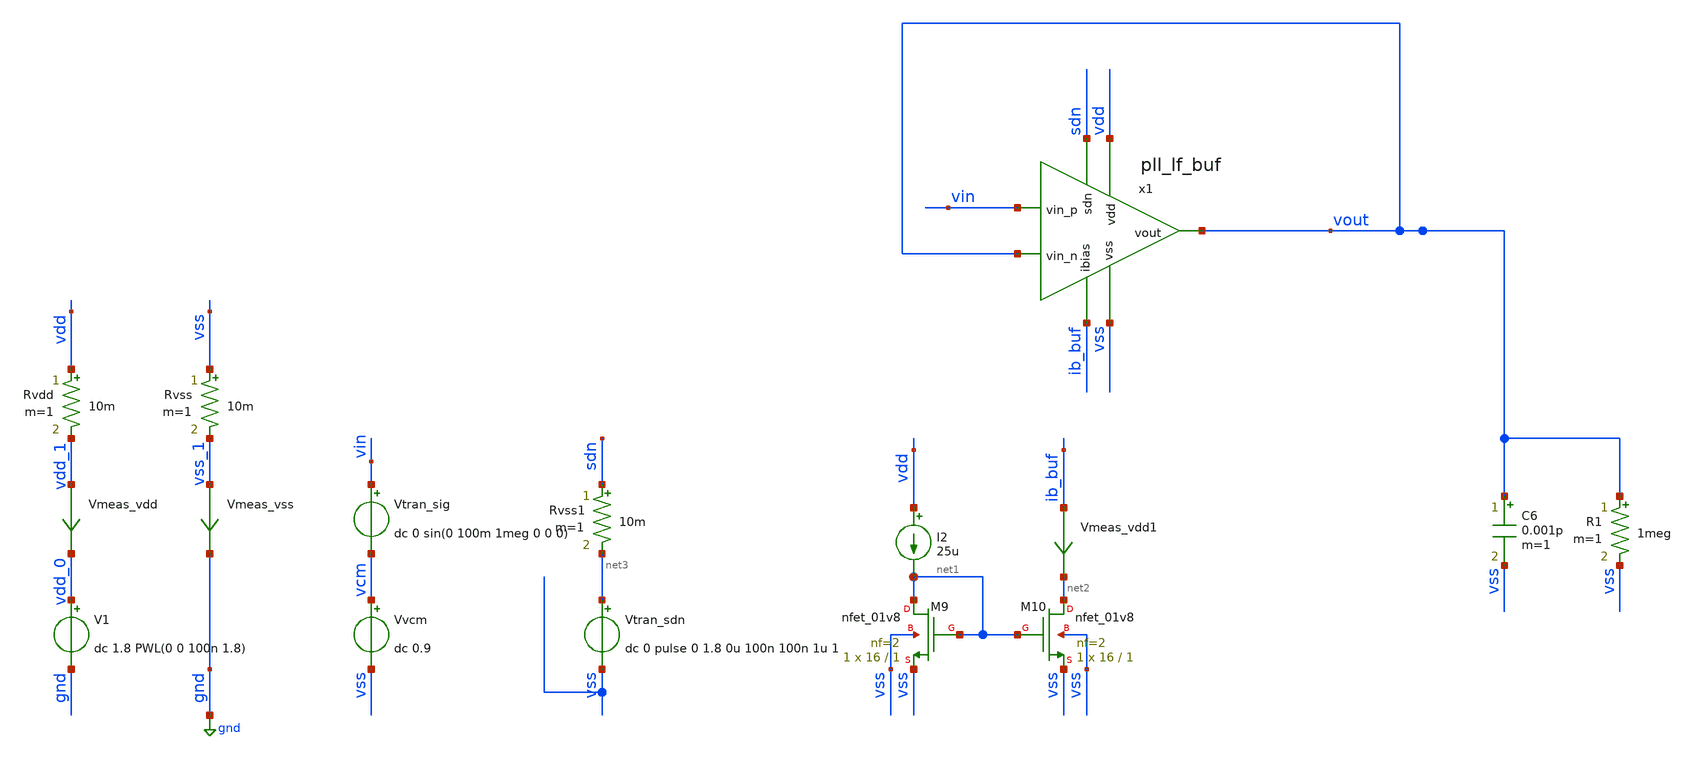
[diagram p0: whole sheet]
** sch_path: pll/pll_lf_buf/simulation/pll_lf_buf_tb_tran.sch
**.subckt pll_lf_buf_tb_tran
Vvcm vcm vss dc 0.9
C6 vout vss 0.001p m=1
Vtran_sig vin vcm dc 0 sin(0 100m 1meg 0 0 0)
Vtran_sdn net3 vss dc 0 pulse 0 1.8 0u 100n 100n 1u 1
V1 vdd_0 gnd dc 1.8 PWL(0 0 100n 1.8)
Vmeas_vdd vdd_1 vdd_0 0
.save i(vmeas_vdd)
Vmeas_vss vss_1 gnd 0
.save i(vmeas_vss)
Rvdd vdd vdd_1 10m m=1
Rvss vss vss_1 10m m=1
I2 vdd net1 25u
R1 vout vss 1meg m=1
Rvss1 sdn net3 10m m=1
XM9 net1 net1 vss vss sky130_fd_pr__nfet_01v8 L=1 W=16 nf=2 ad='int((nf+1)/2) * W/nf * 0.29' as='int((nf+2)/2) * W/nf * 0.29'
+ pd='2*int((nf+1)/2) * (W/nf + 0.29)' ps='2*int((nf+2)/2) * (W/nf + 0.29)' nrd='0.29 / W' nrs='0.29 / W'
+ sa=0 sb=0 sd=0 mult=1 m=1
XM10 net2 net1 vss vss sky130_fd_pr__nfet_01v8 L=1 W=16 nf=2 ad='int((nf+1)/2) * W/nf * 0.29' as='int((nf+2)/2) * W/nf * 0.29'
+ pd='2*int((nf+1)/2) * (W/nf + 0.29)' ps='2*int((nf+2)/2) * (W/nf + 0.29)' nrd='0.29 / W' nrs='0.29 / W'
+ sa=0 sb=0 sd=0 mult=1 m=1
Vmeas_vdd1 ib_buf net2 0
.save i(vmeas_vdd1)
x1 vdd vin sdn vout vout ib_buf vss pll_lf_buf
**** begin user architecture code


.param temp=27

.param ac_on=1
.param stb_on= 0
.param tran_on=0
.param step_on=0

.option savecurrents
*.option rshunt = 1e12
*.option gmin = 1e-24
**.option method=Gear
**.option chgtol=1e-12


*.model switch1 aswitch(cntl_off=0.0 cntl_on=0.1 r_off=1e12 r_on=1.0 log=TRUE)
.model sw SW (ron=0.1 roff=1e12 vt=0.5 vh=0)

.control

* Current mirror
save i(@m.xm9.msky130_fd_pr__nfet_01v8[id])
save @m.xm9.msky130_fd_pr__nfet_01v8[gm]
save v(@m.xm9.msky130_fd_pr__nfet_01v8[vds])
save v(@m.xm9.msky130_fd_pr__nfet_01v8[vgs])
save v(@m.xm9.msky130_fd_pr__nfet_01v8[vth])
save v(@m.xm9.msky130_fd_pr__nfet_01v8[vdsat])

save i(@m.xm10.msky130_fd_pr__nfet_01v8[id])
save @m.xm10.msky130_fd_pr__nfet_01v8[gm]
save v(@m.xm10.msky130_fd_pr__nfet_01v8[vds])
save v(@m.xm10.msky130_fd_pr__nfet_01v8[vgs])
save v(@m.xm10.msky130_fd_pr__nfet_01v8[vth])
save v(@m.xm10.msky130_fd_pr__nfet_01v8[vdsat])


* Main Amplifier
** Main Core OP params
save i(@m.x1.xm1.msky130_fd_pr__pfet_01v8[id])
save @m.x1.xm1.msky130_fd_pr__pfet_01v8[gm]
save v(@m.x1.xm1.msky130_fd_pr__pfet_01v8[vds])
save v(@m.x1.xm1.msky130_fd_pr__pfet_01v8[vgs])
save v(@m.x1.xm1.msky130_fd_pr__pfet_01v8[vth])
save v(@m.x1.xm1.msky130_fd_pr__pfet_01v8[vdsat])

save i(@m.x1.xm2.msky130_fd_pr__pfet_01v8[id])
save @m.x1.xm2.msky130_fd_pr__pfet_01v8[gm]
save v(@m.x1.xm2.msky130_fd_pr__pfet_01v8[vds])
save v(@m.x1.xm2.msky130_fd_pr__pfet_01v8[vgs])
save v(@m.x1.xm2.msky130_fd_pr__pfet_01v8[vth])
save v(@m.x1.xm2.msky130_fd_pr__pfet_01v8[vdsat])

save i(@m.x1.xm3.msky130_fd_pr__pfet_01v8[id])
save @m.x1.xm3.msky130_fd_pr__pfet_01v8[gm]
save v(@m.x1.xm3.msky130_fd_pr__pfet_01v8[vds])
save v(@m.x1.xm3.msky130_fd_pr__pfet_01v8[vgs])
save v(@m.x1.xm3.msky130_fd_pr__pfet_01v8[vth])
save v(@m.x1.xm3.msky130_fd_pr__pfet_01v8[vdsat])

save i(@m.x1.xm4.msky130_fd_pr__pfet_01v8[id])
save @m.x1.xm4.msky130_fd_pr__pfet_01v8[gm]
save v(@m.x1.xm4.msky130_fd_pr__pfet_01v8[vds])
save v(@m.x1.xm4.msky130_fd_pr__pfet_01v8[vgs])
save v(@m.x1.xm4.msky130_fd_pr__pfet_01v8[vth])
save v(@m.x1.xm4.msky130_fd_pr__pfet_01v8[vdsat])

save i(@m.x1.xm5.msky130_fd_pr__pfet_01v8[id])
save @m.x1.xm5.msky130_fd_pr__pfet_01v8[gm]
save v(@m.x1.xm5.msky130_fd_pr__pfet_01v8[vds])
save v(@m.x1.xm5.msky130_fd_pr__pfet_01v8[vgs])
save v(@m.x1.xm5.msky130_fd_pr__pfet_01v8[vth])
save v(@m.x1.xm5.msky130_fd_pr__pfet_01v8[vdsat])

save i(@m.x1.xm6.msky130_fd_pr__pfet_01v8[id])
save @m.x1.xm6.msky130_fd_pr__pfet_01v8[gm]
save v(@m.x1.xm6.msky130_fd_pr__pfet_01v8[vds])
save v(@m.x1.xm6.msky130_fd_pr__pfet_01v8[vgs])
save v(@m.x1.xm6.msky130_fd_pr__pfet_01v8[vth])
save v(@m.x1.xm6.msky130_fd_pr__pfet_01v8[vdsat])

save i(@m.x1.xm7.msky130_fd_pr__nfet_01v8[id])
save @m.x1.xm7.msky130_fd_pr__nfet_01v8[gm]
save v(@m.x1.xm7.msky130_fd_pr__nfet_01v8[vds])
save v(@m.x1.xm7.msky130_fd_pr__nfet_01v8[vgs])
save v(@m.x1.xm7.msky130_fd_pr__nfet_01v8[vth])
save v(@m.x1.xm7.msky130_fd_pr__nfet_01v8[vdsat])

save i(@m.x1.xm8.msky130_fd_pr__nfet_01v8[id])
save @m.x1.xm8.msky130_fd_pr__nfet_01v8[gm]
save v(@m.x1.xm8.msky130_fd_pr__nfet_01v8[vds])
save v(@m.x1.xm8.msky130_fd_pr__nfet_01v8[vgs])
save v(@m.x1.xm8.msky130_fd_pr__nfet_01v8[vth])
save v(@m.x1.xm8.msky130_fd_pr__nfet_01v8[vdsat])

save i(@m.x1.xm9.msky130_fd_pr__nfet_01v8[id])
save @m.x1.xm9.msky130_fd_pr__nfet_01v8[gm]
save v(@m.x1.xm9.msky130_fd_pr__nfet_01v8[vds])
save v(@m.x1.xm9.msky130_fd_pr__nfet_01v8[vgs])
save v(@m.x1.xm9.msky130_fd_pr__nfet_01v8[vth])
save v(@m.x1.xm9.msky130_fd_pr__nfet_01v8[vdsat])

save i(@m.x1.xm10.msky130_fd_pr__nfet_01v8[id])
save @m.x1.xm10.msky130_fd_pr__nfet_01v8[gm]
save v(@m.x1.xm10.msky130_fd_pr__nfet_01v8[vds])
save v(@m.x1.xm10.msky130_fd_pr__nfet_01v8[vgs])
save v(@m.x1.xm10.msky130_fd_pr__nfet_01v8[vth])
save v(@m.x1.xm10.msky130_fd_pr__nfet_01v8[vdsat])

save i(@m.x1.xm11.msky130_fd_pr__pfet_01v8[id])
save @m.x1.xm11.msky130_fd_pr__pfet_01v8[gm]
save v(@m.x1.xm11.msky130_fd_pr__pfet_01v8[vds])
save v(@m.x1.xm11.msky130_fd_pr__pfet_01v8[vgs])
save v(@m.x1.xm11.msky130_fd_pr__pfet_01v8[vth])
save v(@m.x1.xm11.msky130_fd_pr__pfet_01v8[vdsat])

** Biasing
save i(@m.x1.xm12.msky130_fd_pr__pfet_01v8[id])
save @m.x1.xm12.msky130_fd_pr__pfet_01v8[gm]
save v(@m.x1.xm12.msky130_fd_pr__pfet_01v8[vds])
save v(@m.x1.xm12.msky130_fd_pr__pfet_01v8[vgs])
save v(@m.x1.xm12.msky130_fd_pr__pfet_01v8[vth])
save v(@m.x1.xm12.msky130_fd_pr__pfet_01v8[vdsat])

save i(@m.x1.xm13.msky130_fd_pr__pfet_01v8[id])
save @m.x1.xm13.msky130_fd_pr__pfet_01v8[gm]
save v(@m.x1.xm13.msky130_fd_pr__pfet_01v8[vds])
save v(@m.x1.xm13.msky130_fd_pr__pfet_01v8[vgs])
save v(@m.x1.xm13.msky130_fd_pr__pfet_01v8[vth])
save v(@m.x1.xm13.msky130_fd_pr__pfet_01v8[vdsat])

save i(@m.x1.xm14.msky130_fd_pr__pfet_01v8[id])
save @m.x1.xm14.msky130_fd_pr__pfet_01v8[gm]
save v(@m.x1.xm14.msky130_fd_pr__pfet_01v8[vds])
save v(@m.x1.xm14.msky130_fd_pr__pfet_01v8[vgs])
save v(@m.x1.xm14.msky130_fd_pr__pfet_01v8[vth])
save v(@m.x1.xm14.msky130_fd_pr__pfet_01v8[vdsat])

save i(@m.x1.xm15.msky130_fd_pr__pfet_01v8[id])
save @m.x1.xm15.msky130_fd_pr__pfet_01v8[gm]
save v(@m.x1.xm15.msky130_fd_pr__pfet_01v8[vds])
save v(@m.x1.xm15.msky130_fd_pr__pfet_01v8[vgs])
save v(@m.x1.xm15.msky130_fd_pr__pfet_01v8[vth])
save v(@m.x1.xm15.msky130_fd_pr__pfet_01v8[vdsat])

save i(@m.x1.xm23.msky130_fd_pr__nfet_01v8[id])
save @m.x1.xm23.msky130_fd_pr__nfet_01v8[gm]
save v(@m.x1.xm23.msky130_fd_pr__nfet_01v8[vds])
save v(@m.x1.xm23.msky130_fd_pr__nfet_01v8[vgs])
save v(@m.x1.xm23.msky130_fd_pr__nfet_01v8[vth])
save v(@m.x1.xm23.msky130_fd_pr__nfet_01v8[vdsat])

save i(@m.x1.xm24.msky130_fd_pr__pfet_01v8[id])
save @m.x1.xm24.msky130_fd_pr__pfet_01v8[gm]
save v(@m.x1.xm24.msky130_fd_pr__pfet_01v8[vds])
save v(@m.x1.xm24.msky130_fd_pr__pfet_01v8[vgs])
save v(@m.x1.xm24.msky130_fd_pr__pfet_01v8[vth])
save v(@m.x1.xm24.msky130_fd_pr__pfet_01v8[vdsat])


** CMFB OP param
save i(@m.x1.xm28.msky130_fd_pr__pfet_01v8[id])
save @m.x1.xm28.msky130_fd_pr__pfet_01v8[gm]
save v(@m.x1.xm28.msky130_fd_pr__pfet_01v8[vds])
save v(@m.x1.xm28.msky130_fd_pr__pfet_01v8[vgs])
save v(@m.x1.xm28.msky130_fd_pr__pfet_01v8[vth])
save v(@m.x1.xm28.msky130_fd_pr__pfet_01v8[vdsat])

save i(@m.x1.xm29.msky130_fd_pr__pfet_01v8_lvt[id])
save @m.x1.xm29.msky130_fd_pr__pfet_01v8_lvt[gm]
save v(@m.x1.xm29.msky130_fd_pr__pfet_01v8_lvt[vds])
save v(@m.x1.xm29.msky130_fd_pr__pfet_01v8_lvt[vgs])
save v(@m.x1.xm29.msky130_fd_pr__pfet_01v8_lvt[vth])
save v(@m.x1.xm29.msky130_fd_pr__pfet_01v8_lvt[vdsat])

save i(@m.x1.xm30.msky130_fd_pr__pfet_01v8_lvt[id])
save @m.x1.xm30.msky130_fd_pr__pfet_01v8_lvt[gm]
save v(@m.x1.xm30.msky130_fd_pr__pfet_01v8_lvt[vds])
save v(@m.x1.xm30.msky130_fd_pr__pfet_01v8_lvt[vgs])
save v(@m.x1.xm30.msky130_fd_pr__pfet_01v8_lvt[vth])
save v(@m.x1.xm30.msky130_fd_pr__pfet_01v8_lvt[vdsat])

save i(@m.x1.xm31.msky130_fd_pr__pfet_01v8[id])
save @m.x1.xm31.msky130_fd_pr__pfet_01v8[gm]
save v(@m.x1.xm31.msky130_fd_pr__pfet_01v8[vds])
save v(@m.x1.xm31.msky130_fd_pr__pfet_01v8[vgs])
save v(@m.x1.xm31.msky130_fd_pr__pfet_01v8[vth])
save v(@m.x1.xm31.msky130_fd_pr__pfet_01v8[vdsat])

save i(@m.x1.xm32.msky130_fd_pr__pfet_01v8_lvt[id])
save @m.x1.xm32.msky130_fd_pr__pfet_01v8_lvt[gm]
save v(@m.x1.xm32.msky130_fd_pr__pfet_01v8_lvt[vds])
save v(@m.x1.xm32.msky130_fd_pr__pfet_01v8_lvt[vgs])
save v(@m.x1.xm32.msky130_fd_pr__pfet_01v8_lvt[vth])
save v(@m.x1.xm32.msky130_fd_pr__pfet_01v8_lvt[vdsat])

save i(@m.x1.xm33.msky130_fd_pr__pfet_01v8_lvt[id])
save @m.x1.xm33.msky130_fd_pr__pfet_01v8_lvt[gm]
save v(@m.x1.xm33.msky130_fd_pr__pfet_01v8_lvt[vds])
save v(@m.x1.xm33.msky130_fd_pr__pfet_01v8_lvt[vgs])
save v(@m.x1.xm33.msky130_fd_pr__pfet_01v8_lvt[vth])
save v(@m.x1.xm33.msky130_fd_pr__pfet_01v8_lvt[vdsat])

save i(@m.x1.xm34.msky130_fd_pr__nfet_01v8[id])
save @m.x1.xm34.msky130_fd_pr__nfet_01v8[gm]
save v(@m.x1.xm34.msky130_fd_pr__nfet_01v8[vds])
save v(@m.x1.xm34.msky130_fd_pr__nfet_01v8[vgs])
save v(@m.x1.xm34.msky130_fd_pr__nfet_01v8[vth])
save v(@m.x1.xm34.msky130_fd_pr__nfet_01v8[vdsat])

save i(@m.x1.xm35.msky130_fd_pr__nfet_01v8[id])
save @m.x1.xm35.msky130_fd_pr__nfet_01v8[gm]
save v(@m.x1.xm35.msky130_fd_pr__nfet_01v8[vds])
save v(@m.x1.xm35.msky130_fd_pr__nfet_01v8[vgs])
save v(@m.x1.xm35.msky130_fd_pr__nfet_01v8[vth])
save v(@m.x1.xm35.msky130_fd_pr__nfet_01v8[vdsat])

* Gain Booster Pside
** Main core OP parameters
save i(@m.x1.xgbp.xm1.msky130_fd_pr__nfet_01v8[id])
save @m.x1.xgbp.xm1.msky130_fd_pr__nfet_01v8[gm]
save v(@m.x1.xgbp.xm1.msky130_fd_pr__nfet_01v8[vds])
save v(@m.x1.xgbp.xm1.msky130_fd_pr__nfet_01v8[vgs])
save v(@m.x1.xgbp.xm1.msky130_fd_pr__nfet_01v8[vth])
save v(@m.x1.xgbp.xm1.msky130_fd_pr__nfet_01v8[vdsat])

save i(@m.x1.xgbp.xm2.msky130_fd_pr__nfet_01v8[id])
save @m.x1.xgbp.xm2.msky130_fd_pr__nfet_01v8[gm]
save v(@m.x1.xgbp.xm2.msky130_fd_pr__nfet_01v8[vds])
save v(@m.x1.xgbp.xm2.msky130_fd_pr__nfet_01v8[vgs])
save v(@m.x1.xgbp.xm2.msky130_fd_pr__nfet_01v8[vth])
save v(@m.x1.xgbp.xm2.msky130_fd_pr__nfet_01v8[vdsat])

save i(@m.x1.xgbp.xm3.msky130_fd_pr__nfet_01v8[id])
save @m.x1.xgbp.xm3.msky130_fd_pr__nfet_01v8[gm]
save v(@m.x1.xgbp.xm3.msky130_fd_pr__nfet_01v8[vds])
save v(@m.x1.xgbp.xm3.msky130_fd_pr__nfet_01v8[vgs])
save v(@m.x1.xgbp.xm3.msky130_fd_pr__nfet_01v8[vth])
save v(@m.x1.xgbp.xm3.msky130_fd_pr__nfet_01v8[vdsat])

save i(@m.x1.xgbp.xm4.msky130_fd_pr__pfet_01v8[id])
save @m.x1.xgbp.xm4.msky130_fd_pr__pfet_01v8[gm]
save v(@m.x1.xgbp.xm4.msky130_fd_pr__pfet_01v8[vds])
save v(@m.x1.xgbp.xm4.msky130_fd_pr__pfet_01v8[vgs])
save v(@m.x1.xgbp.xm4.msky130_fd_pr__pfet_01v8[vth])
save v(@m.x1.xgbp.xm4.msky130_fd_pr__pfet_01v8[vdsat])

save i(@m.x1.xgbp.xm5.msky130_fd_pr__pfet_01v8[id])
save @m.x1.xgbp.xm5.msky130_fd_pr__pfet_01v8[gm]
save v(@m.x1.xgbp.xm5.msky130_fd_pr__pfet_01v8[vds])
save v(@m.x1.xgbp.xm5.msky130_fd_pr__pfet_01v8[vgs])
save v(@m.x1.xgbp.xm5.msky130_fd_pr__pfet_01v8[vth])
save v(@m.x1.xgbp.xm5.msky130_fd_pr__pfet_01v8[vdsat])

save i(@m.x1.xgbp.xm6.msky130_fd_pr__pfet_01v8[id])
save @m.x1.xgbp.xm6.msky130_fd_pr__pfet_01v8[gm]
save v(@m.x1.xgbp.xm6.msky130_fd_pr__pfet_01v8[vds])
save v(@m.x1.xgbp.xm6.msky130_fd_pr__pfet_01v8[vgs])
save v(@m.x1.xgbp.xm6.msky130_fd_pr__pfet_01v8[vth])
save v(@m.x1.xgbp.xm6.msky130_fd_pr__pfet_01v8[vdsat])

save i(@m.x1.xgbp.xm7.msky130_fd_pr__pfet_01v8[id])
save @m.x1.xgbp.xm7.msky130_fd_pr__pfet_01v8[gm]
save v(@m.x1.xgbp.xm7.msky130_fd_pr__pfet_01v8[vds])
save v(@m.x1.xgbp.xm7.msky130_fd_pr__pfet_01v8[vgs])
save v(@m.x1.xgbp.xm7.msky130_fd_pr__pfet_01v8[vth])
save v(@m.x1.xgbp.xm7.msky130_fd_pr__pfet_01v8[vdsat])

save i(@m.x1.xgbp.xm8.msky130_fd_pr__nfet_01v8[id])
save @m.x1.xgbp.xm8.msky130_fd_pr__nfet_01v8[gm]
save v(@m.x1.xgbp.xm8.msky130_fd_pr__nfet_01v8[vds])
save v(@m.x1.xgbp.xm8.msky130_fd_pr__nfet_01v8[vgs])
save v(@m.x1.xgbp.xm8.msky130_fd_pr__nfet_01v8[vth])
save v(@m.x1.xgbp.xm8.msky130_fd_pr__nfet_01v8[vdsat])

save i(@m.x1.xgbp.xm9.msky130_fd_pr__nfet_01v8[id])
save @m.x1.xgbp.xm9.msky130_fd_pr__nfet_01v8[gm]
save v(@m.x1.xgbp.xm9.msky130_fd_pr__nfet_01v8[vds])
save v(@m.x1.xgbp.xm9.msky130_fd_pr__nfet_01v8[vgs])
save v(@m.x1.xgbp.xm9.msky130_fd_pr__nfet_01v8[vth])
save v(@m.x1.xgbp.xm9.msky130_fd_pr__nfet_01v8[vdsat])

save i(@m.x1.xgbp.xm10.msky130_fd_pr__nfet_01v8[id])
save @m.x1.xgbp.xm10.msky130_fd_pr__nfet_01v8[gm]
save v(@m.x1.xgbp.xm10.msky130_fd_pr__nfet_01v8[vds])
save v(@m.x1.xgbp.xm10.msky130_fd_pr__nfet_01v8[vgs])
save v(@m.x1.xgbp.xm10.msky130_fd_pr__nfet_01v8[vth])
save v(@m.x1.xgbp.xm10.msky130_fd_pr__nfet_01v8[vdsat])

save i(@m.x1.xgbp.xm11.msky130_fd_pr__nfet_01v8[id])
save @m.x1.xgbp.xm11.msky130_fd_pr__nfet_01v8[gm]
save v(@m.x1.xgbp.xm11.msky130_fd_pr__nfet_01v8[vds])
save v(@m.x1.xgbp.xm11.msky130_fd_pr__nfet_01v8[vgs])
save v(@m.x1.xgbp.xm11.msky130_fd_pr__nfet_01v8[vth])
save v(@m.x1.xgbp.xm11.msky130_fd_pr__nfet_01v8[vdsat])


** CMFB OP param
save i(@m.x1.xgbp.xm28.msky130_fd_pr__pfet_01v8[id])
save @m.x1.xgbp.xm28.msky130_fd_pr__pfet_01v8[gm]
save v(@m.x1.xgbp.xm28.msky130_fd_pr__pfet_01v8[vds])
save v(@m.x1.xgbp.xm28.msky130_fd_pr__pfet_01v8[vgs])
save v(@m.x1.xgbp.xm28.msky130_fd_pr__pfet_01v8[vth])
save v(@m.x1.xgbp.xm28.msky130_fd_pr__pfet_01v8[vdsat])

save i(@m.x1.xgbp.xm29.msky130_fd_pr__pfet_01v8_lvt[id])
save @m.x1.xgbp.xm29.msky130_fd_pr__pfet_01v8_lvt[gm]
save v(@m.x1.xgbp.xm29.msky130_fd_pr__pfet_01v8_lvt[vds])
save v(@m.x1.xgbp.xm29.msky130_fd_pr__pfet_01v8_lvt[vgs])
save v(@m.x1.xgbp.xm29.msky130_fd_pr__pfet_01v8_lvt[vth])
save v(@m.x1.xgbp.xm29.msky130_fd_pr__pfet_01v8_lvt[vdsat])

save i(@m.x1.xgbp.xm30.msky130_fd_pr__pfet_01v8_lvt[id])
save @m.x1.xgbp.xm30.msky130_fd_pr__pfet_01v8_lvt[gm]
save v(@m.x1.xgbp.xm30.msky130_fd_pr__pfet_01v8_lvt[vds])
save v(@m.x1.xgbp.xm30.msky130_fd_pr__pfet_01v8_lvt[vgs])
save v(@m.x1.xgbp.xm30.msky130_fd_pr__pfet_01v8_lvt[vth])
save v(@m.x1.xgbp.xm30.msky130_fd_pr__pfet_01v8_lvt[vdsat])

save i(@m.x1.xgbp.xm31.msky130_fd_pr__pfet_01v8[id])
save @m.x1.xgbp.xm31.msky130_fd_pr__pfet_01v8[gm]
save v(@m.x1.xgbp.xm31.msky130_fd_pr__pfet_01v8[vds])
save v(@m.x1.xgbp.xm31.msky130_fd_pr__pfet_01v8[vgs])
save v(@m.x1.xgbp.xm31.msky130_fd_pr__pfet_01v8[vth])
save v(@m.x1.xgbp.xm31.msky130_fd_pr__pfet_01v8[vdsat])

save i(@m.x1.xgbp.xm32.msky130_fd_pr__pfet_01v8_lvt[id])
save @m.x1.xgbp.xm32.msky130_fd_pr__pfet_01v8_lvt[gm]
save v(@m.x1.xgbp.xm32.msky130_fd_pr__pfet_01v8_lvt[vds])
save v(@m.x1.xgbp.xm32.msky130_fd_pr__pfet_01v8_lvt[vgs])
save v(@m.x1.xgbp.xm32.msky130_fd_pr__pfet_01v8_lvt[vth])
save v(@m.x1.xgbp.xm32.msky130_fd_pr__pfet_01v8_lvt[vdsat])

save i(@m.x1.xgbp.xm33.msky130_fd_pr__pfet_01v8_lvt[id])
save @m.x1.xgbp.xm33.msky130_fd_pr__pfet_01v8_lvt[gm]
save v(@m.x1.xgbp.xm33.msky130_fd_pr__pfet_01v8_lvt[vds])
save v(@m.x1.xgbp.xm33.msky130_fd_pr__pfet_01v8_lvt[vgs])
save v(@m.x1.xgbp.xm33.msky130_fd_pr__pfet_01v8_lvt[vth])
save v(@m.x1.xgbp.xm33.msky130_fd_pr__pfet_01v8_lvt[vdsat])

save i(@m.x1.xgbp.xm34.msky130_fd_pr__nfet_01v8[id])
save @m.x1.xgbp.xm34.msky130_fd_pr__nfet_01v8[gm]
save v(@m.x1.xgbp.xm34.msky130_fd_pr__nfet_01v8[vds])
save v(@m.x1.xgbp.xm34.msky130_fd_pr__nfet_01v8[vgs])
save v(@m.x1.xgbp.xm34.msky130_fd_pr__nfet_01v8[vth])
save v(@m.x1.xgbp.xm34.msky130_fd_pr__nfet_01v8[vdsat])

save i(@m.x1.xgbp.xm35.msky130_fd_pr__nfet_01v8[id])
save @m.x1.xgbp.xm35.msky130_fd_pr__nfet_01v8[gm]
save v(@m.x1.xgbp.xm35.msky130_fd_pr__nfet_01v8[vds])
save v(@m.x1.xgbp.xm35.msky130_fd_pr__nfet_01v8[vgs])
save v(@m.x1.xgbp.xm35.msky130_fd_pr__nfet_01v8[vth])
save v(@m.x1.xgbp.xm35.msky130_fd_pr__nfet_01v8[vdsat])


* #################################################################
* #
* #                         OPERATING POINT
* #
* #################################################################
save all
save v(vin)
save v(vout)

op
set filetype=binary
write pll_lf_buf_tb_tran.raw all


* #################################################################
* #
* #                          AC SIMULATION
* #
* #################################################################
*alterparam ac_on=1
*alterparam stb_on=0
*alterparam tran_on=0
*alterparam step_on=0
*reset
*save all
*save v(vin)
*save v(vout)
*
*ac dec 100 1 1T
*set filetype=ascii
*write  pll_lf_buf_tb_ac_tran.raw all
*
*plot dB(v(vout)/v(vin))


* #################################################################
* #
* #                 TRANSIENT SINE WAVE REGIME
* #
* #################################################################
alterparam ac_on=0
alterparam stb_on=0
alterparam tran_on=1
alterparam step_on=0
reset
save all
save v(vin)
save v(vout)

set imp_ac = @Rin[r]
alter @Rin[r]=1e12

*tran 100n 6m 5.96m 100n
tran 0.100n 10u 0u 0.100n
*tran 100n 100m 100n
set filetype=ascii
write pll_lf_buf_tb_tran_tran.raw all

alter @Rin[r]=imp_ac

plot v(vin) v(vout)


* #################################################################
* #
* #                   TRANSIENT STEP RESPONSE
* #
* #################################################################
*alterparam ac_on = 0
*alterparam stb_on = 0
*alterparam tran_on = 0
*alterparam step_on = 1
*reset
*save all
*save v(vin)
*save v(vout)
*
*set imp_ac = @Rin[r]
*alter @Rin[r]=1e12
*
*tran 0.1n 0.9u 0.8u
*set filetype=ascii
*write pll_lf_buf_tb_step.raw all
*
*alter @Rin[r]=imp_ac
*
*plot v(vin) v(vout)

.endc



.options wnflag=1
.include $::SKYWATER_MODELS/cells/nfet_01v8/sky130_fd_pr__nfet_01v8__tt.corner.spice
.include $::SKYWATER_MODELS/cells/nfet_01v8_lvt/sky130_fd_pr__nfet_01v8_lvt__tt.corner.spice
.include $::SKYWATER_MODELS/cells/pfet_01v8/sky130_fd_pr__pfet_01v8__tt.corner.spice
.include $::SKYWATER_MODELS/cells/nfet_03v3_nvt/sky130_fd_pr__nfet_03v3_nvt__tt.corner.spice
.include $::SKYWATER_MODELS/cells/nfet_05v0_nvt/sky130_fd_pr__nfet_05v0_nvt__tt.corner.spice
.include $::SKYWATER_MODELS/cells/esd_nfet_01v8/sky130_fd_pr__esd_nfet_01v8__tt.corner.spice
.include $::SKYWATER_MODELS/cells/pfet_01v8_lvt/sky130_fd_pr__pfet_01v8_lvt__tt.corner.spice
.include $::SKYWATER_MODELS/cells/pfet_01v8_hvt/sky130_fd_pr__pfet_01v8_hvt__tt.corner.spice
.include $::SKYWATER_MODELS/cells/esd_pfet_g5v0d10v5/sky130_fd_pr__esd_pfet_g5v0d10v5__tt.corner.spice
.include $::SKYWATER_MODELS/cells/pfet_g5v0d10v5/sky130_fd_pr__pfet_g5v0d10v5__tt.corner.spice
.include $::SKYWATER_MODELS/cells/pfet_g5v0d16v0/sky130_fd_pr__pfet_g5v0d16v0__tt.corner.spice
.include $::SKYWATER_MODELS/cells/nfet_g5v0d10v5/sky130_fd_pr__nfet_g5v0d10v5__tt.corner.spice
.include $::SKYWATER_MODELS/cells/nfet_g5v0d16v0/sky130_fd_pr__nfet_g5v0d16v0__tt_discrete.corner.spice
.include $::SKYWATER_MODELS/cells/esd_nfet_g5v0d10v5/sky130_fd_pr__esd_nfet_g5v0d10v5__tt.corner.spice
.include $::SKYWATER_MODELS/models/corners/tt/nonfet.spice
* Mismatch parameters
.include $::SKYWATER_MODELS/cells/nfet_01v8/sky130_fd_pr__nfet_01v8__mismatch.corner.spice
.include $::SKYWATER_MODELS/cells/pfet_01v8/sky130_fd_pr__pfet_01v8__mismatch.corner.spice
.include $::SKYWATER_MODELS/cells/nfet_01v8_lvt/sky130_fd_pr__nfet_01v8_lvt__mismatch.corner.spice
.include $::SKYWATER_MODELS/cells/pfet_01v8_lvt/sky130_fd_pr__pfet_01v8_lvt__mismatch.corner.spice
.include $::SKYWATER_MODELS/cells/pfet_01v8_hvt/sky130_fd_pr__pfet_01v8_hvt__mismatch.corner.spice
.include $::SKYWATER_MODELS/cells/nfet_g5v0d10v5/sky130_fd_pr__nfet_g5v0d10v5__mismatch.corner.spice
.include $::SKYWATER_MODELS/cells/pfet_g5v0d10v5/sky130_fd_pr__pfet_g5v0d10v5__mismatch.corner.spice
.include $::SKYWATER_MODELS/cells/nfet_05v0_nvt/sky130_fd_pr__nfet_05v0_nvt__mismatch.corner.spice
.include $::SKYWATER_MODELS/cells/nfet_03v3_nvt/sky130_fd_pr__nfet_03v3_nvt__mismatch.corner.spice
* Resistor$::SKYWATER_MODELS/Capacitor
.include $::SKYWATER_MODELS/models/r+c/res_typical__cap_typical.spice
.include $::SKYWATER_MODELS/models/r+c/res_typical__cap_typical__lin.spice
* Special cells
.include $::SKYWATER_MODELS/models/corners/tt/specialized_cells.spice
* All models
.include $::SKYWATER_MODELS/models/all.spice
* Corner
.include $::SKYWATER_MODELS/models/corners/tt/rf.spice

**** end user architecture code
**.ends

* expanding   symbol:  test_jens/pll/pll_lf_buf/pll_lf_buf.sym # of pins=7
** sym_path: pll/pll_lf_buf/xschem/pll_lf_buf.sym
** sch_path: pll/pll_lf_buf/xschem/pll_lf_buf.sch
.subckt pll_lf_buf vdd vin_p sdn vin_n vout ibias vss
*.iopin vss
*.iopin vdd
*.ipin vin_p
*.ipin vin_n
*.iopin ibias
*.opin vout
*.ipin sdn
XM1 net4 vin_p net1 vdd sky130_fd_pr__pfet_01v8 L=0.15 W=16 nf=2 ad='int((nf+1)/2) * W/nf * 0.29' as='int((nf+2)/2) * W/nf * 0.29'
+ pd='2*int((nf+1)/2) * (W/nf + 0.29)' ps='2*int((nf+2)/2) * (W/nf + 0.29)' nrd='0.29 / W' nrs='0.29 / W'
+ sa=0 sb=0 sd=0 mult=8 m=8
XM2 net5 vin_n net1 vdd sky130_fd_pr__pfet_01v8 L=0.15 W=16 nf=2 ad='int((nf+1)/2) * W/nf * 0.29' as='int((nf+2)/2) * W/nf * 0.29'
+ pd='2*int((nf+1)/2) * (W/nf + 0.29)' ps='2*int((nf+2)/2) * (W/nf + 0.29)' nrd='0.29 / W' nrs='0.29 / W'
+ sa=0 sb=0 sd=0 mult=8 m=8
XM3 vbn vbp_casc net2 vdd sky130_fd_pr__pfet_01v8 L=0.3 W=16 nf=2 ad='int((nf+1)/2) * W/nf * 0.29' as='int((nf+2)/2) * W/nf * 0.29'
+ pd='2*int((nf+1)/2) * (W/nf + 0.29)' ps='2*int((nf+2)/2) * (W/nf + 0.29)' nrd='0.29 / W' nrs='0.29 / W'
+ sa=0 sb=0 sd=0 mult=8 m=8
XM4 vout vbp_casc net3 vdd sky130_fd_pr__pfet_01v8 L=0.3 W=16 nf=2 ad='int((nf+1)/2) * W/nf * 0.29' as='int((nf+2)/2) * W/nf * 0.29'
+ pd='2*int((nf+1)/2) * (W/nf + 0.29)' ps='2*int((nf+2)/2) * (W/nf + 0.29)' nrd='0.29 / W' nrs='0.29 / W'
+ sa=0 sb=0 sd=0 mult=8 m=8
XM5 net2 vbp vdd vdd sky130_fd_pr__pfet_01v8 L=0.3 W=16 nf=2 ad='int((nf+1)/2) * W/nf * 0.29' as='int((nf+2)/2) * W/nf * 0.29'
+ pd='2*int((nf+1)/2) * (W/nf + 0.29)' ps='2*int((nf+2)/2) * (W/nf + 0.29)' nrd='0.29 / W' nrs='0.29 / W'
+ sa=0 sb=0 sd=0 mult=8 m=8
XM6 net3 vbp vdd vdd sky130_fd_pr__pfet_01v8 L=0.3 W=16 nf=2 ad='int((nf+1)/2) * W/nf * 0.29' as='int((nf+2)/2) * W/nf * 0.29'
+ pd='2*int((nf+1)/2) * (W/nf + 0.29)' ps='2*int((nf+2)/2) * (W/nf + 0.29)' nrd='0.29 / W' nrs='0.29 / W'
+ sa=0 sb=0 sd=0 mult=8 m=8
XM7 vbn vbn_casc net4 vss sky130_fd_pr__nfet_01v8 L=0.3 W=8 nf=2 ad='int((nf+1)/2) * W/nf * 0.29' as='int((nf+2)/2) * W/nf * 0.29'
+ pd='2*int((nf+1)/2) * (W/nf + 0.29)' ps='2*int((nf+2)/2) * (W/nf + 0.29)' nrd='0.29 / W' nrs='0.29 / W'
+ sa=0 sb=0 sd=0 mult=8 m=8
XM8 vout vbn_casc net5 vss sky130_fd_pr__nfet_01v8 L=0.3 W=8 nf=2 ad='int((nf+1)/2) * W/nf * 0.29' as='int((nf+2)/2) * W/nf * 0.29'
+ pd='2*int((nf+1)/2) * (W/nf + 0.29)' ps='2*int((nf+2)/2) * (W/nf + 0.29)' nrd='0.29 / W' nrs='0.29 / W'
+ sa=0 sb=0 sd=0 mult=8 m=8
XM9 net4 vbn vss vss sky130_fd_pr__nfet_01v8 L=0.3 W=8 nf=2 ad='int((nf+1)/2) * W/nf * 0.29' as='int((nf+2)/2) * W/nf * 0.29'
+ pd='2*int((nf+1)/2) * (W/nf + 0.29)' ps='2*int((nf+2)/2) * (W/nf + 0.29)' nrd='0.29 / W' nrs='0.29 / W'
+ sa=0 sb=0 sd=0 mult=8 m=8
XM10 net5 vbn vss vss sky130_fd_pr__nfet_01v8 L=0.3 W=8 nf=2 ad='int((nf+1)/2) * W/nf * 0.29' as='int((nf+2)/2) * W/nf * 0.29'
+ pd='2*int((nf+1)/2) * (W/nf + 0.29)' ps='2*int((nf+2)/2) * (W/nf + 0.29)' nrd='0.29 / W' nrs='0.29 / W'
+ sa=0 sb=0 sd=0 mult=8 m=8
XM11 net1 vbp vdd vdd sky130_fd_pr__pfet_01v8 L=0.3 W=8 nf=2 ad='int((nf+1)/2) * W/nf * 0.29' as='int((nf+2)/2) * W/nf * 0.29'
+ pd='2*int((nf+1)/2) * (W/nf + 0.29)' ps='2*int((nf+2)/2) * (W/nf + 0.29)' nrd='0.29 / W' nrs='0.29 / W'
+ sa=0 sb=0 sd=0 mult=8 m=8
XM12 net9 net10 vdd vdd sky130_fd_pr__pfet_01v8 L=0.3 W=16 nf=2 ad='int((nf+1)/2) * W/nf * 0.29' as='int((nf+2)/2) * W/nf * 0.29'
+ pd='2*int((nf+1)/2) * (W/nf + 0.29)' ps='2*int((nf+2)/2) * (W/nf + 0.29)' nrd='0.29 / W' nrs='0.29 / W'
+ sa=0 sb=0 sd=0 mult=1 m=1
XM13 net6 vbp vdd vdd sky130_fd_pr__pfet_01v8 L=0.3 W=16 nf=2 ad='int((nf+1)/2) * W/nf * 0.29' as='int((nf+2)/2) * W/nf * 0.29'
+ pd='2*int((nf+1)/2) * (W/nf + 0.29)' ps='2*int((nf+2)/2) * (W/nf + 0.29)' nrd='0.29 / W' nrs='0.29 / W'
+ sa=0 sb=0 sd=0 mult=1 m=1
XM14 net10 net8 net9 vdd sky130_fd_pr__pfet_01v8 L=0.3 W=16 nf=2 ad='int((nf+1)/2) * W/nf * 0.29' as='int((nf+2)/2) * W/nf * 0.29'
+ pd='2*int((nf+1)/2) * (W/nf + 0.29)' ps='2*int((nf+2)/2) * (W/nf + 0.29)' nrd='0.29 / W' nrs='0.29 / W'
+ sa=0 sb=0 sd=0 mult=1 m=1
XM15 vbn_casc vbp_casc net6 vdd sky130_fd_pr__pfet_01v8 L=0.3 W=16 nf=2 ad='int((nf+1)/2) * W/nf * 0.29'
+ as='int((nf+2)/2) * W/nf * 0.29' pd='2*int((nf+1)/2) * (W/nf + 0.29)' ps='2*int((nf+2)/2) * (W/nf + 0.29)'
+ nrd='0.29 / W' nrs='0.29 / W' sa=0 sb=0 sd=0 mult=1 m=1
XM16 vbn_casc vbn_casc vss vss sky130_fd_pr__nfet_01v8 L=1.2 W=4 nf=2 ad='int((nf+1)/2) * W/nf * 0.29'
+ as='int((nf+2)/2) * W/nf * 0.29' pd='2*int((nf+1)/2) * (W/nf + 0.29)' ps='2*int((nf+2)/2) * (W/nf + 0.29)'
+ nrd='0.29 / W' nrs='0.29 / W' sa=0 sb=0 sd=0 mult=1 m=1
XM17 net7 vbn_casc vss vss sky130_fd_pr__nfet_01v8 L=1.2 W=4 nf=2 ad='int((nf+1)/2) * W/nf * 0.29' as='int((nf+2)/2) * W/nf * 0.29'
+ pd='2*int((nf+1)/2) * (W/nf + 0.29)' ps='2*int((nf+2)/2) * (W/nf + 0.29)' nrd='0.29 / W' nrs='0.29 / W'
+ sa=0 sb=0 sd=0 mult=1 m=1
XM18 net7 net7 vdd vdd sky130_fd_pr__pfet_01v8 L=1.2 W=16 nf=2 ad='int((nf+1)/2) * W/nf * 0.29' as='int((nf+2)/2) * W/nf * 0.29'
+ pd='2*int((nf+1)/2) * (W/nf + 0.29)' ps='2*int((nf+2)/2) * (W/nf + 0.29)' nrd='0.29 / W' nrs='0.29 / W'
+ sa=0 sb=0 sd=0 mult=1 m=1
XM19 vbn sdn vss vss sky130_fd_pr__nfet_01v8 L=0.3 W=1 nf=1 ad='int((nf+1)/2) * W/nf * 0.29' as='int((nf+2)/2) * W/nf * 0.29'
+ pd='2*int((nf+1)/2) * (W/nf + 0.29)' ps='2*int((nf+2)/2) * (W/nf + 0.29)' nrd='0.29 / W' nrs='0.29 / W'
+ sa=0 sb=0 sd=0 mult=1 m=1
XM20 vbn_casc sdn vss vss sky130_fd_pr__nfet_01v8 L=0.3 W=1 nf=1 ad='int((nf+1)/2) * W/nf * 0.29' as='int((nf+2)/2) * W/nf * 0.29'
+ pd='2*int((nf+1)/2) * (W/nf + 0.29)' ps='2*int((nf+2)/2) * (W/nf + 0.29)' nrd='0.29 / W' nrs='0.29 / W'
+ sa=0 sb=0 sd=0 mult=1 m=1
XM21 vbp sdn_b vdd vdd sky130_fd_pr__pfet_01v8 L=0.3 W=1 nf=1 ad='int((nf+1)/2) * W/nf * 0.29' as='int((nf+2)/2) * W/nf * 0.29'
+ pd='2*int((nf+1)/2) * (W/nf + 0.29)' ps='2*int((nf+2)/2) * (W/nf + 0.29)' nrd='0.29 / W' nrs='0.29 / W'
+ sa=0 sb=0 sd=0 mult=1 m=1
XM22 vbp_casc sdn_b vdd vdd sky130_fd_pr__pfet_01v8 L=0.3 W=1 nf=1 ad='int((nf+1)/2) * W/nf * 0.29' as='int((nf+2)/2) * W/nf * 0.29'
+ pd='2*int((nf+1)/2) * (W/nf + 0.29)' ps='2*int((nf+2)/2) * (W/nf + 0.29)' nrd='0.29 / W' nrs='0.29 / W'
+ sa=0 sb=0 sd=0 mult=1 m=1
XM23 net8 sdn_b ibias vss sky130_fd_pr__nfet_01v8 L=0.15 W=4 nf=8 ad='int((nf+1)/2) * W/nf * 0.29' as='int((nf+2)/2) * W/nf * 0.29'
+ pd='2*int((nf+1)/2) * (W/nf + 0.29)' ps='2*int((nf+2)/2) * (W/nf + 0.29)' nrd='0.29 / W' nrs='0.29 / W'
+ sa=0 sb=0 sd=0 mult=1 m=1
**** begin user architecture code

.include $::SKYWATER_STDCELLS/cells/inv/sky130_fd_sc_hd__inv_1.spice
.include $::SKYWATER_STDCELLS/cells/inv/sky130_fd_sc_hd__inv_2.spice
.include $::SKYWATER_STDCELLS/cells/inv/sky130_fd_sc_hd__inv_4.spice
.include $::SKYWATER_STDCELLS/cells/inv/sky130_fd_sc_hd__inv_8.spice

**** end user architecture code
x1 sdn vss vss vdd vdd sdn_b sky130_fd_sc_hd__inv_1
R1 net10 net8 8k m=1
R2 vbp_casc net8 1 m=1
R3 vbp net10 1 m=1
XM24 ibias sdn net8 vdd sky130_fd_pr__pfet_01v8 L=0.15 W=12 nf=8 ad='int((nf+1)/2) * W/nf * 0.29' as='int((nf+2)/2) * W/nf * 0.29'
+ pd='2*int((nf+1)/2) * (W/nf + 0.29)' ps='2*int((nf+2)/2) * (W/nf + 0.29)' nrd='0.29 / W' nrs='0.29 / W'
+ sa=0 sb=0 sd=0 mult=1 m=1
.ends

.GLOBAL gnd
.end
